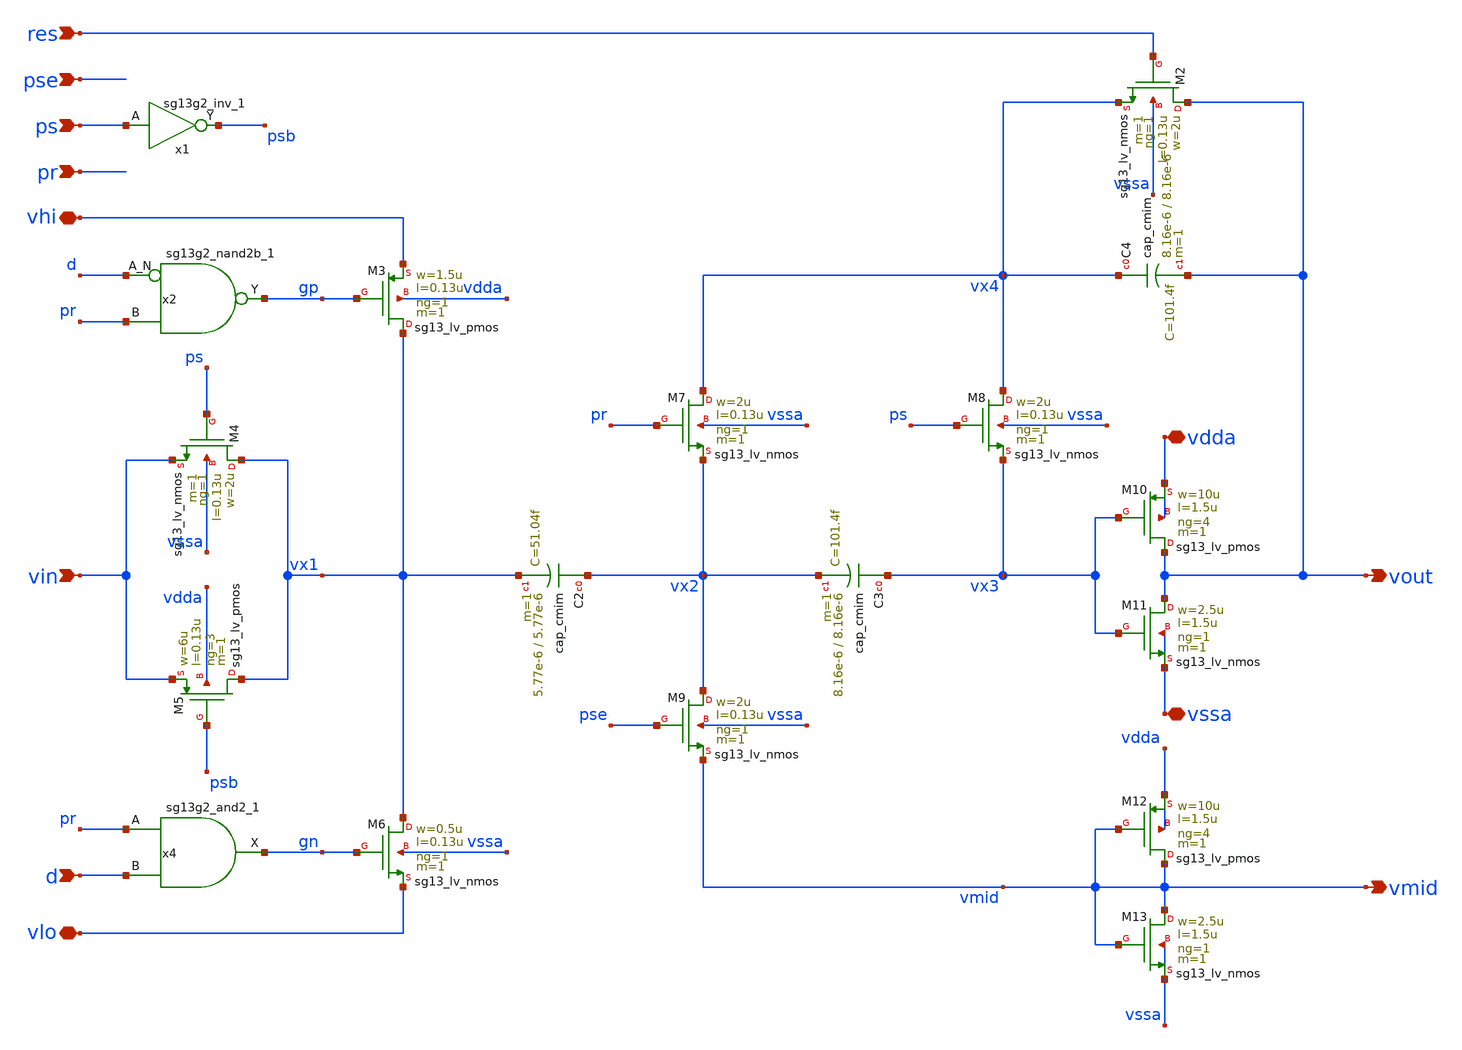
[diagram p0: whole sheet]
** sch_path: 5_Design/4_Layout/Team 1/xschem/stage_t1.sch
* IHP-GmbH/IHP-Open-PDK/ihp-sg13g2/libs.tech/xschem/sg13g2_stdcells/sg13g2_nand2b_1.sch:
* Copyright 2023 IHP PDK Authors
* Licensed under the Apache License, Version 2.0 (the "License");
**.subckt stage_t1 res pse ps pr vhi vin d vlo vdda vssa vout vmid
*.ipin res
*.ipin pse
*.ipin ps
*.ipin pr
*.iopin vhi
*.ipin vin
*.ipin d
*.iopin vlo
*.iopin vdda
*.iopin vssa
*.opin vout
*.opin vmid
x1 psb ps VDD VSS sg13g2_inv_1
x2 gp d pr VDD VSS sg13g2_nand2b_1
XM2 vout res vx4 vssa sg13_lv_nmos w=2u l=0.13u ng=1 m=1 mm_ok=1
XM3 vx1 gp vhi vdda sg13_lv_pmos w=1.5u l=0.13u ng=1 m=1 mm_ok=1
XM4 vx1 ps vin vssa sg13_lv_nmos w=2u l=0.13u ng=1 m=1 mm_ok=1
XM5 vx1 psb vin vdda sg13_lv_pmos w=6u l=0.13u ng=3 m=1 mm_ok=1
XC2 vx2 vx1 cap_cmim w=5.77e-6 l=5.77e-6 m=1 mm_ok=1
x4 gn pr d VDD VSS sg13g2_and2_1
XM6 vx1 gn vlo vssa sg13_lv_nmos w=0.5u l=0.13u ng=1 m=1 mm_ok=1
XC3 vx3 vx2 cap_cmim w=8.16e-6 l=8.16e-6 m=1 mm_ok=1
XM7 vx4 pr vx2 vssa sg13_lv_nmos w=2u l=0.13u ng=1 m=1 mm_ok=1
XM8 vx4 ps vx3 vssa sg13_lv_nmos w=2u l=0.13u ng=1 m=1 mm_ok=1
XC4 vx4 vout cap_cmim w=8.16e-6 l=8.16e-6 m=1 mm_ok=1
XM9 vx2 pse vmid vssa sg13_lv_nmos w=2u l=0.13u ng=1 m=1 mm_ok=1
XM10 vout vx3 vdda vdda sg13_lv_pmos w=10u l=1.5u ng=4 m=1 mm_ok=1
XM11 vout vx3 vssa vssa sg13_lv_nmos w=2.5u l=1.5u ng=1 m=1 mm_ok=1
XM12 vmid vmid vdda vdda sg13_lv_pmos w=10u l=1.5u ng=4 m=1 mm_ok=1
XM13 vmid vmid vssa vssa sg13_lv_nmos w=2.5u l=1.5u ng=1 m=1 mm_ok=1
**.ends

* expanding   symbol:  sg13g2_stdcells/sg13g2_inv_1.sym # of pins=2
** sym_path: sg13g2_stdcells/sg13g2_inv_1.sym
** sch_path: sg13g2_stdcells/sg13g2_inv_1.sch
.subckt sg13g2_inv_1 Y A VDD VSS
*.opin Y
*.ipin A
*.iopin VDD
*.iopin VSS
XM1 Y A VSS VSS sg13_lv_nmos w=740.00n l=130.00n ng=1 m=1 mm_ok=1
XM2 Y A VDD VDD sg13_lv_pmos w=1.12u l=130.00n ng=1 m=1 mm_ok=1
.ends


* expanding   symbol:  sg13g2_stdcells/sg13g2_nand2b_1.sym # of pins=3
** sym_path: sg13g2_stdcells/sg13g2_nand2b_1.sym
** sch_path: sg13g2_stdcells/sg13g2_nand2b_1.sch
.subckt sg13g2_nand2b_1 Y A_N B VDD VSS
*.opin Y
*.ipin B
*.ipin A_N
*.iopin VDD
*.iopin VSS
XM1 net1 A_N VSS VSS sg13_lv_nmos w=550.00n l=130.00n ng=1 m=1 mm_ok=1
XM2 Y net1 net2 VSS sg13_lv_nmos w=740.00n l=130.00n ng=1 m=1 mm_ok=1
XM3 net2 B VSS VSS sg13_lv_nmos w=740.00n l=130.00n ng=1 m=1 mm_ok=1
XM4 Y B VDD VDD sg13_lv_pmos w=1.12u l=130.00n ng=1 m=1 mm_ok=1
XM5 net1 A_N VDD VDD sg13_lv_pmos w=840.00n l=130.00n ng=1 m=1 mm_ok=1
XM6 Y net1 VDD VDD sg13_lv_pmos w=1.12u l=130.00n ng=1 m=1 mm_ok=1
.ends


* expanding   symbol:  sg13g2_stdcells/sg13g2_and2_1.sym # of pins=3
** sym_path: sg13g2_stdcells/sg13g2_and2_1.sym
** sch_path: sg13g2_stdcells/sg13g2_and2_1.sch
.subckt sg13g2_and2_1 X A B VDD VSS
*.ipin A
*.ipin B
*.opin X
*.iopin VDD
*.iopin VSS
XM1 net1 A net2 VSS sg13_lv_nmos w=640.00n l=130.00n ng=1 m=1 mm_ok=1
XM2 net2 B VSS VSS sg13_lv_nmos w=640.00n l=130.00n ng=1 m=1 mm_ok=1
XM3 X net1 VSS VSS sg13_lv_nmos w=740.00n l=130.00n ng=1 m=1 mm_ok=1
XM4 net1 B VDD VDD sg13_lv_pmos w=840.00n l=130.00n ng=1 m=1 mm_ok=1
XM5 net1 A VDD VDD sg13_lv_pmos w=840.00n l=130.00n ng=1 m=1 mm_ok=1
XM6 X net1 VDD VDD sg13_lv_pmos w=1.12u l=130.00n ng=1 m=1 mm_ok=1
.ends

.end
